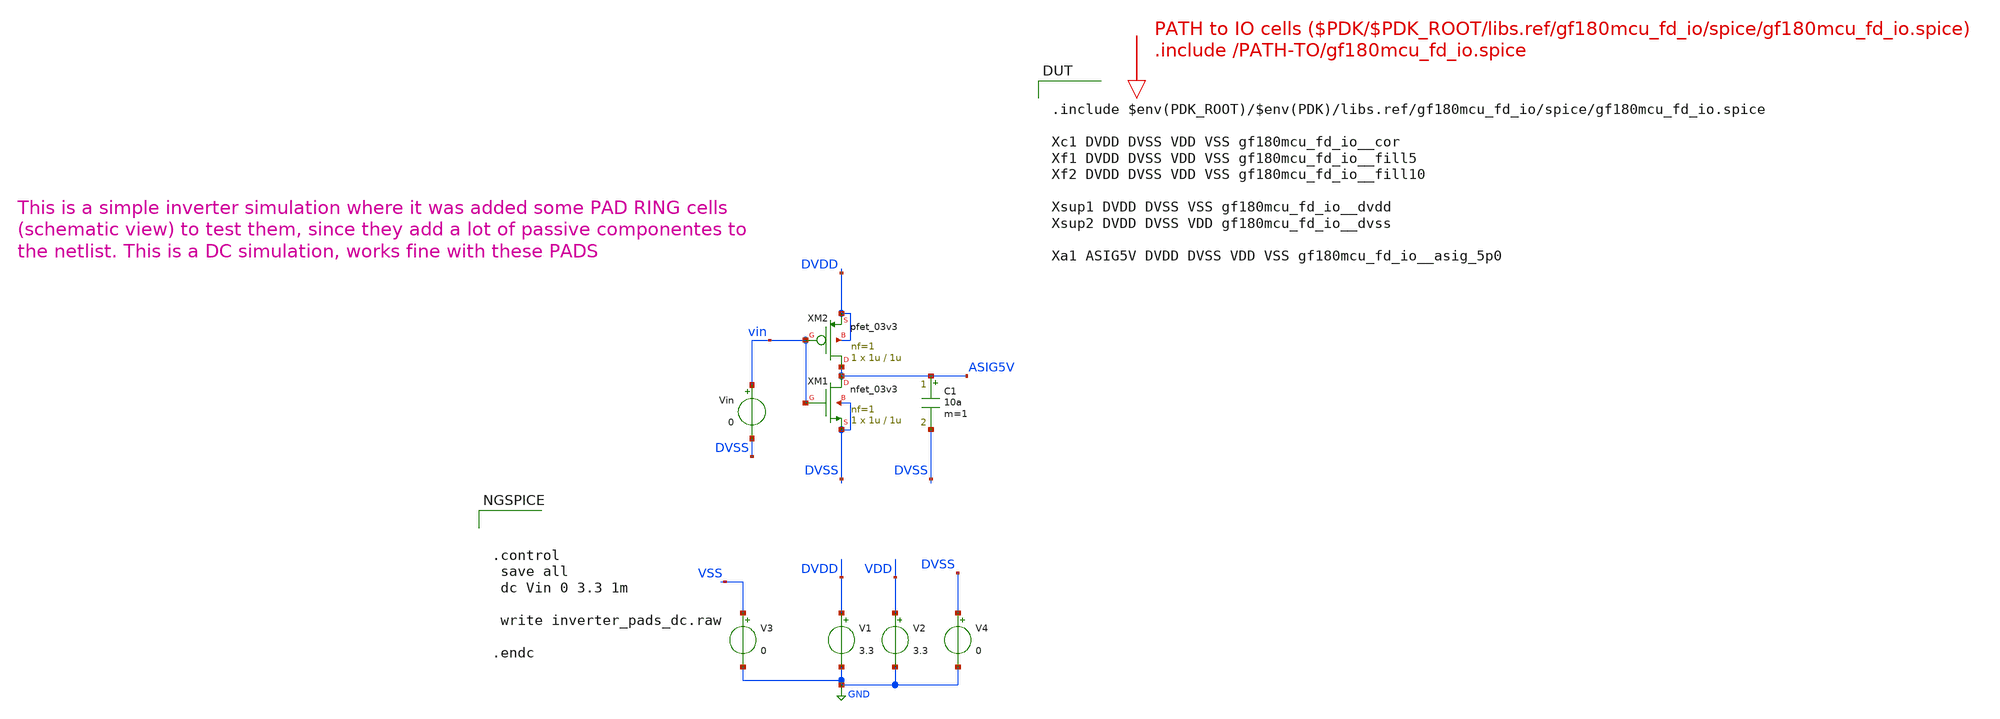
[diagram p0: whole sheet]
** sch_path: padframe/inverter_pads_dc/test/inverter_pads_dc.sch

.include $env(PDK_ROOT)/$env(PDK)/libs.tech/ngspice/design.ngspice
.lib $env(PDK_ROOT)/$env(PDK)/libs.tech/ngspice/sm141064.ngspice typical
.lib $env(PDK_ROOT)/$env(PDK)/libs.tech/ngspice/sm141064.ngspice diode_typical
.lib $env(PDK_ROOT)/$env(PDK)/libs.tech/ngspice/sm141064.ngspice mimcap_typical
.lib $env(PDK_ROOT)/$env(PDK)/libs.tech/ngspice/sm141064.ngspice moscap_typical
.lib $env(PDK_ROOT)/$env(PDK)/libs.tech/ngspice/sm141064.ngspice cap_mim
.lib $env(PDK_ROOT)/$env(PDK)/libs.tech/ngspice/sm141064.ngspice res_typical
.lib $env(PDK_ROOT)/$env(PDK)/libs.tech/ngspice/smbb000149.ngspice typical

**.subckt inverter_pads_dc
V1 DVDD GND 3.3
V2 VDD GND 3.3
Vin vin DVSS 0
C1 ASIG5V DVSS 10a m=1
V3 VSS GND 0
V4 DVSS GND 0
XM1 ASIG5V vin DVSS DVSS nfet_03v3 L=1u W=1u nf=1 ad='int((nf+1)/2) * W/nf * 0.18u' as='int((nf+2)/2) * W/nf * 0.18u'
+ pd='2*int((nf+1)/2) * (W/nf + 0.18u)' ps='2*int((nf+2)/2) * (W/nf + 0.18u)' nrd='0.18u / W' nrs='0.18u / W'
+ sa=0 sb=0 sd=0 m=1
XM2 ASIG5V vin DVDD DVDD pfet_03v3 L=1u W=1u nf=1 ad='int((nf+1)/2) * W/nf * 0.18u' as='int((nf+2)/2) * W/nf * 0.18u'
+ pd='2*int((nf+1)/2) * (W/nf + 0.18u)' ps='2*int((nf+2)/2) * (W/nf + 0.18u)' nrd='0.18u / W' nrs='0.18u / W'
+ sa=0 sb=0 sd=0 m=1
**** begin user architecture code

.include $env(PDK_ROOT)/$env(PDK)/libs.ref/gf180mcu_fd_io/spice/gf180mcu_fd_io.spice

Xc1 DVDD DVSS VDD VSS gf180mcu_fd_io__cor
Xf1 DVDD DVSS VDD VSS gf180mcu_fd_io__fill5
Xf2 DVDD DVSS VDD VSS gf180mcu_fd_io__fill10

Xsup1 DVDD DVSS VSS gf180mcu_fd_io__dvdd
Xsup2 DVDD DVSS VDD gf180mcu_fd_io__dvss

Xa1 ASIG5V DVDD DVSS VDD VSS gf180mcu_fd_io__asig_5p0





.control
 save all
 dc Vin 0 3.3 1m

 write inverter_pads_dc.raw

.endc



**** end user architecture code
**.ends
.GLOBAL GND
.end
